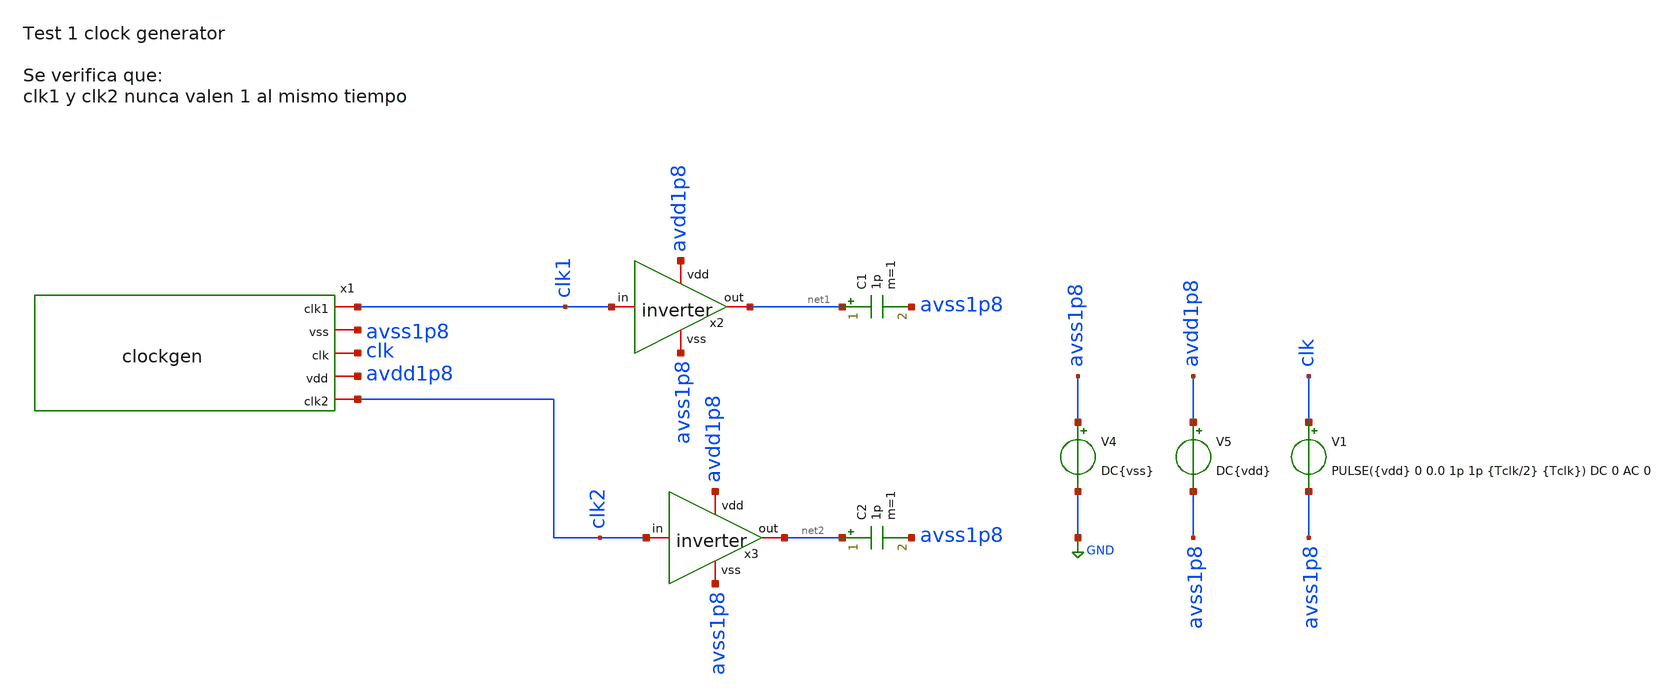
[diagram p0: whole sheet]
** sch_path: designs/sch/tests/test1_clockgen.sch
**.subckt test1_clockgen
x2 avdd1p8 net1 clk1 avss1p8 inverter
V4 avss1p8 GND DC{vss}
V5 avdd1p8 avss1p8 DC{vdd}
C1 net1 avss1p8 1p m=1
V1 clk avss1p8 PULSE({vdd} 0 0.0 1p 1p {Tclk/2} {Tclk}) DC 0 AC 0
x3 avdd1p8 net2 clk2 avss1p8 inverter
C2 net2 avss1p8 1p m=1
x1 clk1 avss1p8 clk avdd1p8 clk2 clockgen
**** begin user architecture code


* Circuit Parameters
.param vdd = 1.8
.param vss = 0.0
.param Tclk = 5n
.options TEMP = 65.0

* Include Models
.lib /foss/pdks/sky130A/libs.tech/ngspice/sky130.lib.spice TT

* OP Parameters & Singals to save
.save all

* Simulations
.control
  tran 0.001n 10n
  setplot tran1
  plot clk v(clk1)+2 v(clk2)+4
reset
.endc

.end


**** end user architecture code
**.ends

* expanding   symbol:  /foss/designs/sch/inverter.sym # of pins=4
** sym_path: designs/inverter.sym
** sch_path: designs/inverter.sch
.subckt inverter vdd out in vss
*.iopin out
*.iopin vss
*.iopin vdd
*.iopin in
XM2 out in vss vss sky130_fd_pr__nfet_01v8 L=0.15 W=0.75 nf=1 ad='int((nf+1)/2) * W/nf * 0.29' as='int((nf+2)/2) * W/nf * 0.29'
+ pd='2*int((nf+1)/2) * (W/nf + 0.29)' ps='2*int((nf+2)/2) * (W/nf + 0.29)' nrd='0.29 / W' nrs='0.29 / W'
+ sa=0 sb=0 sd=0 mult=1 m=1
XM1 out in vdd vdd sky130_fd_pr__pfet_01v8 L=0.15 W=1.5 nf=1 ad='int((nf+1)/2) * W/nf * 0.29' as='int((nf+2)/2) * W/nf * 0.29'
+ pd='2*int((nf+1)/2) * (W/nf + 0.29)' ps='2*int((nf+2)/2) * (W/nf + 0.29)' nrd='0.29 / W' nrs='0.29 / W'
+ sa=0 sb=0 sd=0 mult=1 m=1
.ends


* expanding   symbol:  /foss/designs/sch/clockgen.sym # of pins=5
** sym_path: designs/sch/clockgen.sym
** sch_path: designs/sch/clockgen.sch
.subckt clockgen clk1 vss clk vdd clk2
*.iopin vss
*.iopin vdd
*.iopin clk1
*.iopin clk2
*.iopin clk
x1 vdd net4 clk vss inverter
x2 vdd net2 net1 clk2 vss nor
x3 vdd net3 clk1 net4 vss nor
x4 vdd net7 clk vss inverter
x6 vdd net5 net2 vss inverter
x7 vdd net6 net3 vss inverter
x5 vdd clk1 net5 vss inverter
x8 vdd clk2 net6 vss inverter
x9 vdd net1 net7 vss inverter
.ends


* expanding   symbol:  /foss/designs/sch/nor.sym # of pins=5
** sym_path: designs/sch/nor.sym
** sch_path: designs/sch/nor.sch
.subckt nor vdd Z A B vss
*.iopin A
*.iopin B
*.iopin vdd
*.iopin Z
*.iopin vss
XM1 Z A vss vss sky130_fd_pr__nfet_01v8 L=0.15 W=0.75 nf=1 ad='int((nf+1)/2) * W/nf * 0.29' as='int((nf+2)/2) * W/nf * 0.29'
+ pd='2*int((nf+1)/2) * (W/nf + 0.29)' ps='2*int((nf+2)/2) * (W/nf + 0.29)' nrd='0.29 / W' nrs='0.29 / W'
+ sa=0 sb=0 sd=0 mult=1 m=1
XM4 net1 B vdd vdd sky130_fd_pr__pfet_01v8 L=0.15 W=3 nf=1 ad='int((nf+1)/2) * W/nf * 0.29' as='int((nf+2)/2) * W/nf * 0.29'
+ pd='2*int((nf+1)/2) * (W/nf + 0.29)' ps='2*int((nf+2)/2) * (W/nf + 0.29)' nrd='0.29 / W' nrs='0.29 / W'
+ sa=0 sb=0 sd=0 mult=1 m=1
XM2 Z B vss vss sky130_fd_pr__nfet_01v8 L=0.15 W=0.75 nf=1 ad='int((nf+1)/2) * W/nf * 0.29' as='int((nf+2)/2) * W/nf * 0.29'
+ pd='2*int((nf+1)/2) * (W/nf + 0.29)' ps='2*int((nf+2)/2) * (W/nf + 0.29)' nrd='0.29 / W' nrs='0.29 / W'
+ sa=0 sb=0 sd=0 mult=1 m=1
XM3 Z A net1 vdd sky130_fd_pr__pfet_01v8 L=0.15 W=3 nf=1 ad='int((nf+1)/2) * W/nf * 0.29' as='int((nf+2)/2) * W/nf * 0.29'
+ pd='2*int((nf+1)/2) * (W/nf + 0.29)' ps='2*int((nf+2)/2) * (W/nf + 0.29)' nrd='0.29 / W' nrs='0.29 / W'
+ sa=0 sb=0 sd=0 mult=1 m=1
.ends

.GLOBAL GND
.end
